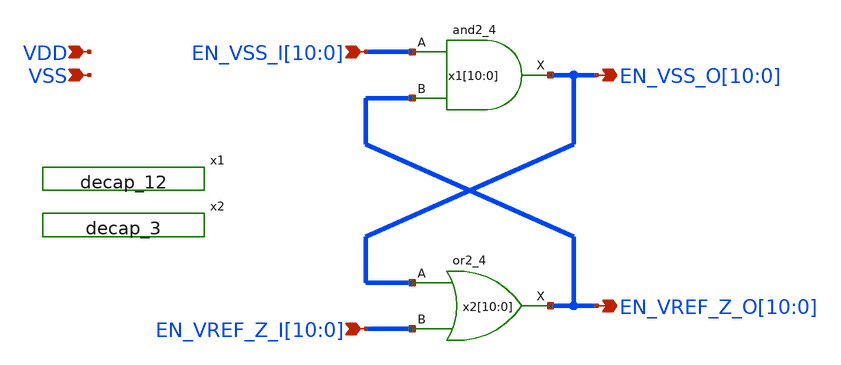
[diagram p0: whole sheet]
** sch_path: schematic/subcells/break_before_make/break_before_make.sch
**.subckt break_before_make
*+ EN_VSS_I[10],EN_VSS_I[9],EN_VSS_I[8],EN_VSS_I[7],EN_VSS_I[6],EN_VSS_I[5],EN_VSS_I[4],EN_VSS_I[3],EN_VSS_I[2],EN_VSS_I[1],EN_VSS_I[0]
*+ EN_VREF_Z_I[10],EN_VREF_Z_I[9],EN_VREF_Z_I[8],EN_VREF_Z_I[7],EN_VREF_Z_I[6],EN_VREF_Z_I[5],EN_VREF_Z_I[4],EN_VREF_Z_I[3],EN_VREF_Z_I[2],EN_VREF_Z_I[1],EN_VREF_Z_I[0] VDD VSS
*+ EN_VSS_O[10],EN_VSS_O[9],EN_VSS_O[8],EN_VSS_O[7],EN_VSS_O[6],EN_VSS_O[5],EN_VSS_O[4],EN_VSS_O[3],EN_VSS_O[2],EN_VSS_O[1],EN_VSS_O[0]
*+ EN_VREF_Z_O[10],EN_VREF_Z_O[9],EN_VREF_Z_O[8],EN_VREF_Z_O[7],EN_VREF_Z_O[6],EN_VREF_Z_O[5],EN_VREF_Z_O[4],EN_VREF_Z_O[3],EN_VREF_Z_O[2],EN_VREF_Z_O[1],EN_VREF_Z_O[0]
*.ipin
*+ EN_VSS_I[10],EN_VSS_I[9],EN_VSS_I[8],EN_VSS_I[7],EN_VSS_I[6],EN_VSS_I[5],EN_VSS_I[4],EN_VSS_I[3],EN_VSS_I[2],EN_VSS_I[1],EN_VSS_I[0]
*.ipin
*+ EN_VREF_Z_I[10],EN_VREF_Z_I[9],EN_VREF_Z_I[8],EN_VREF_Z_I[7],EN_VREF_Z_I[6],EN_VREF_Z_I[5],EN_VREF_Z_I[4],EN_VREF_Z_I[3],EN_VREF_Z_I[2],EN_VREF_Z_I[1],EN_VREF_Z_I[0]
*.ipin VDD
*.ipin VSS
*.opin
*+ EN_VSS_O[10],EN_VSS_O[9],EN_VSS_O[8],EN_VSS_O[7],EN_VSS_O[6],EN_VSS_O[5],EN_VSS_O[4],EN_VSS_O[3],EN_VSS_O[2],EN_VSS_O[1],EN_VSS_O[0]
*.opin
*+ EN_VREF_Z_O[10],EN_VREF_Z_O[9],EN_VREF_Z_O[8],EN_VREF_Z_O[7],EN_VREF_Z_O[6],EN_VREF_Z_O[5],EN_VREF_Z_O[4],EN_VREF_Z_O[3],EN_VREF_Z_O[2],EN_VREF_Z_O[1],EN_VREF_Z_O[0]
x1[10] EN_VSS_I[10] EN_VREF_Z_O[10] VSS VSS VDD VDD EN_VSS_O[10] sky130_fd_sc_hd__and2_4
x1[9] EN_VSS_I[9] EN_VREF_Z_O[9] VSS VSS VDD VDD EN_VSS_O[9] sky130_fd_sc_hd__and2_4
x1[8] EN_VSS_I[8] EN_VREF_Z_O[8] VSS VSS VDD VDD EN_VSS_O[8] sky130_fd_sc_hd__and2_4
x1[7] EN_VSS_I[7] EN_VREF_Z_O[7] VSS VSS VDD VDD EN_VSS_O[7] sky130_fd_sc_hd__and2_4
x1[6] EN_VSS_I[6] EN_VREF_Z_O[6] VSS VSS VDD VDD EN_VSS_O[6] sky130_fd_sc_hd__and2_4
x1[5] EN_VSS_I[5] EN_VREF_Z_O[5] VSS VSS VDD VDD EN_VSS_O[5] sky130_fd_sc_hd__and2_4
x1[4] EN_VSS_I[4] EN_VREF_Z_O[4] VSS VSS VDD VDD EN_VSS_O[4] sky130_fd_sc_hd__and2_4
x1[3] EN_VSS_I[3] EN_VREF_Z_O[3] VSS VSS VDD VDD EN_VSS_O[3] sky130_fd_sc_hd__and2_4
x1[2] EN_VSS_I[2] EN_VREF_Z_O[2] VSS VSS VDD VDD EN_VSS_O[2] sky130_fd_sc_hd__and2_4
x1[1] EN_VSS_I[1] EN_VREF_Z_O[1] VSS VSS VDD VDD EN_VSS_O[1] sky130_fd_sc_hd__and2_4
x1[0] EN_VSS_I[0] EN_VREF_Z_O[0] VSS VSS VDD VDD EN_VSS_O[0] sky130_fd_sc_hd__and2_4
x2[10] EN_VSS_O[10] EN_VREF_Z_I[10] VSS VSS VDD VDD EN_VREF_Z_O[10] sky130_fd_sc_hd__or2_4
x2[9] EN_VSS_O[9] EN_VREF_Z_I[9] VSS VSS VDD VDD EN_VREF_Z_O[9] sky130_fd_sc_hd__or2_4
x2[8] EN_VSS_O[8] EN_VREF_Z_I[8] VSS VSS VDD VDD EN_VREF_Z_O[8] sky130_fd_sc_hd__or2_4
x2[7] EN_VSS_O[7] EN_VREF_Z_I[7] VSS VSS VDD VDD EN_VREF_Z_O[7] sky130_fd_sc_hd__or2_4
x2[6] EN_VSS_O[6] EN_VREF_Z_I[6] VSS VSS VDD VDD EN_VREF_Z_O[6] sky130_fd_sc_hd__or2_4
x2[5] EN_VSS_O[5] EN_VREF_Z_I[5] VSS VSS VDD VDD EN_VREF_Z_O[5] sky130_fd_sc_hd__or2_4
x2[4] EN_VSS_O[4] EN_VREF_Z_I[4] VSS VSS VDD VDD EN_VREF_Z_O[4] sky130_fd_sc_hd__or2_4
x2[3] EN_VSS_O[3] EN_VREF_Z_I[3] VSS VSS VDD VDD EN_VREF_Z_O[3] sky130_fd_sc_hd__or2_4
x2[2] EN_VSS_O[2] EN_VREF_Z_I[2] VSS VSS VDD VDD EN_VREF_Z_O[2] sky130_fd_sc_hd__or2_4
x2[1] EN_VSS_O[1] EN_VREF_Z_I[1] VSS VSS VDD VDD EN_VREF_Z_O[1] sky130_fd_sc_hd__or2_4
x2[0] EN_VSS_O[0] EN_VREF_Z_I[0] VSS VSS VDD VDD EN_VREF_Z_O[0] sky130_fd_sc_hd__or2_4
x1 VSS VSS VDD VDD sky130_fd_sc_hd__decap_12
x2 VSS VSS VDD VDD sky130_fd_sc_hd__decap_3
**.ends
.end
